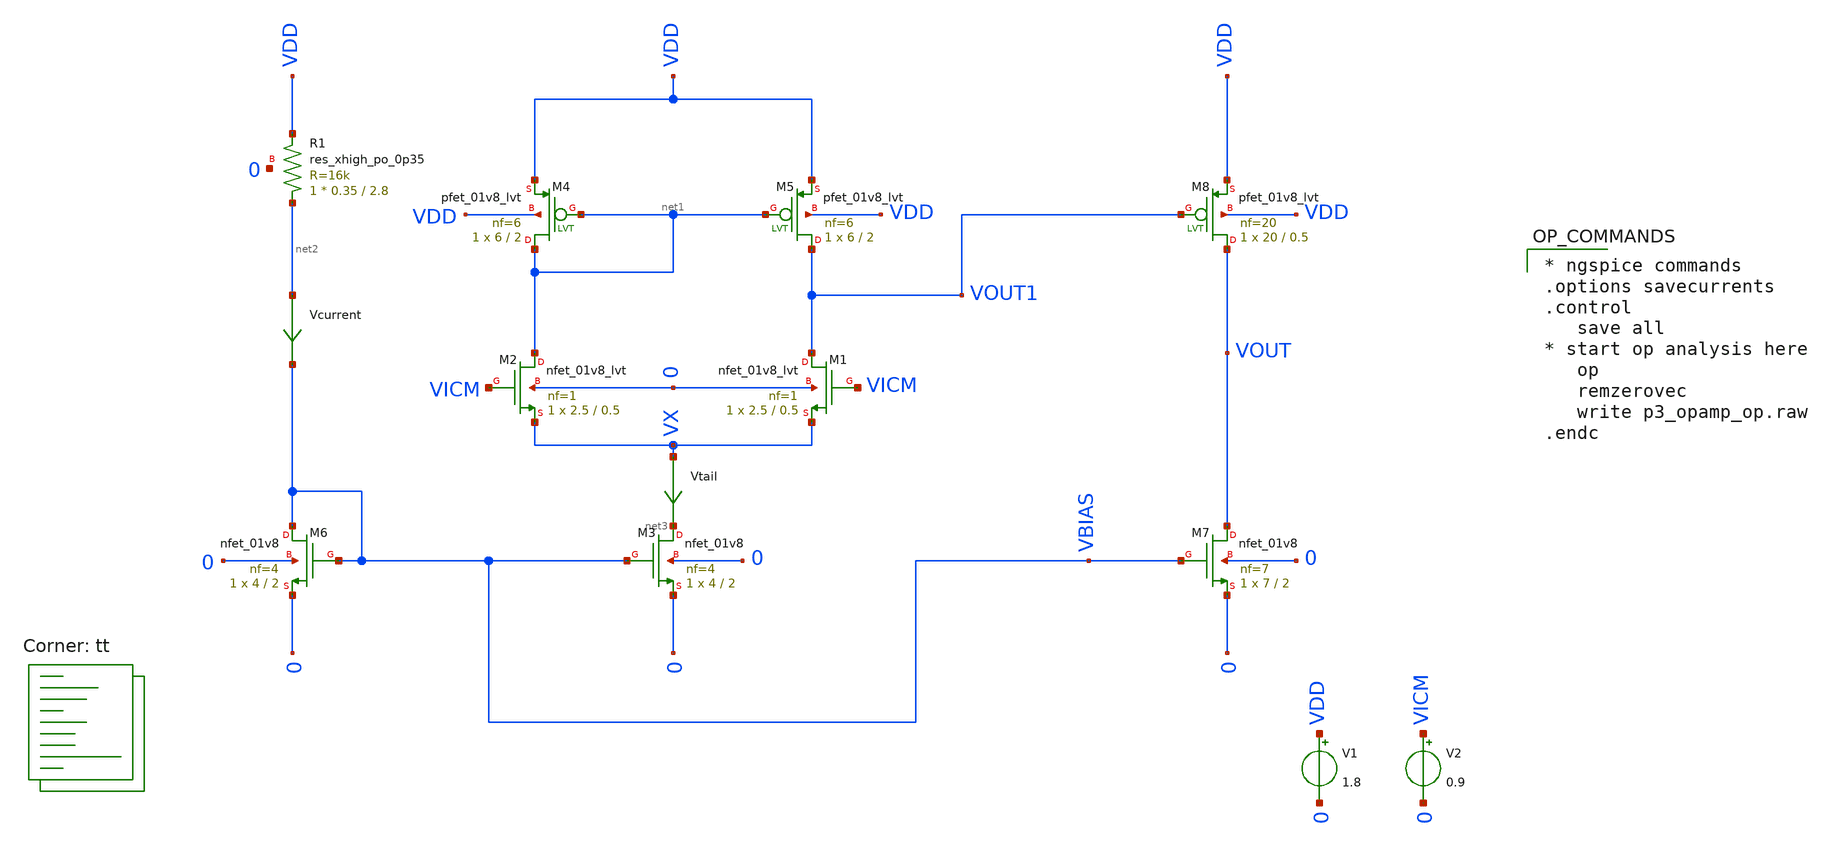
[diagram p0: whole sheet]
** sch_path: xschem/p3_opamp_op.sch
**.subckt p3_opamp_op
XM3 net3 VBIAS 0 0 sky130_fd_pr__nfet_01v8 L=2 W=4 nf=4 ad='int((nf+1)/2) * W/nf * 0.29' as='int((nf+2)/2) * W/nf * 0.29'
+ pd='2*int((nf+1)/2) * (W/nf + 0.29)' ps='2*int((nf+2)/2) * (W/nf + 0.29)' nrd='0.29 / W' nrs='0.29 / W'
+ sa=0 sb=0 sd=0 mult=1 m=1
XM6 VBIAS VBIAS 0 0 sky130_fd_pr__nfet_01v8 L=2 W=4 nf=4 ad='int((nf+1)/2) * W/nf * 0.29' as='int((nf+2)/2) * W/nf * 0.29'
+ pd='2*int((nf+1)/2) * (W/nf + 0.29)' ps='2*int((nf+2)/2) * (W/nf + 0.29)' nrd='0.29 / W' nrs='0.29 / W'
+ sa=0 sb=0 sd=0 mult=1 m=1
XM7 VOUT VBIAS 0 0 sky130_fd_pr__nfet_01v8 L=2 W=7 nf=7 ad='int((nf+1)/2) * W/nf * 0.29' as='int((nf+2)/2) * W/nf * 0.29'
+ pd='2*int((nf+1)/2) * (W/nf + 0.29)' ps='2*int((nf+2)/2) * (W/nf + 0.29)' nrd='0.29 / W' nrs='0.29 / W'
+ sa=0 sb=0 sd=0 mult=1 m=1
V1 VDD 0 1.8
V2 VICM 0 0.9
XR1 net2 VDD 0 sky130_fd_pr__res_xhigh_po_0p35 L=2.8 mult=1 m=1
Vcurrent net2 VBIAS 0
.save i(vcurrent)
Vtail VX net3 0
.save i(vtail)
XM2 net1 VICM VX 0 sky130_fd_pr__nfet_01v8_lvt L=0.5 W=2.5 nf=1 ad='int((nf+1)/2) * W/nf * 0.29' as='int((nf+2)/2) * W/nf * 0.29'
+ pd='2*int((nf+1)/2) * (W/nf + 0.29)' ps='2*int((nf+2)/2) * (W/nf + 0.29)' nrd='0.29 / W' nrs='0.29 / W'
+ sa=0 sb=0 sd=0 mult=1 m=1
XM1 VOUT1 VICM VX 0 sky130_fd_pr__nfet_01v8_lvt L=0.5 W=2.5 nf=1 ad='int((nf+1)/2) * W/nf * 0.29' as='int((nf+2)/2) * W/nf * 0.29'
+ pd='2*int((nf+1)/2) * (W/nf + 0.29)' ps='2*int((nf+2)/2) * (W/nf + 0.29)' nrd='0.29 / W' nrs='0.29 / W'
+ sa=0 sb=0 sd=0 mult=1 m=1
XM4 net1 net1 VDD VDD sky130_fd_pr__pfet_01v8_lvt L=2 W=6 nf=6 ad='int((nf+1)/2) * W/nf * 0.29' as='int((nf+2)/2) * W/nf * 0.29'
+ pd='2*int((nf+1)/2) * (W/nf + 0.29)' ps='2*int((nf+2)/2) * (W/nf + 0.29)' nrd='0.29 / W' nrs='0.29 / W'
+ sa=0 sb=0 sd=0 mult=1 m=1
XM5 VOUT1 net1 VDD VDD sky130_fd_pr__pfet_01v8_lvt L=2 W=6 nf=6 ad='int((nf+1)/2) * W/nf * 0.29' as='int((nf+2)/2) * W/nf * 0.29'
+ pd='2*int((nf+1)/2) * (W/nf + 0.29)' ps='2*int((nf+2)/2) * (W/nf + 0.29)' nrd='0.29 / W' nrs='0.29 / W'
+ sa=0 sb=0 sd=0 mult=1 m=1
XM8 VOUT VOUT1 VDD VDD sky130_fd_pr__pfet_01v8_lvt L=0.5 W=20 nf=20 ad='int((nf+1)/2) * W/nf * 0.29'
+ as='int((nf+2)/2) * W/nf * 0.29' pd='2*int((nf+1)/2) * (W/nf + 0.29)' ps='2*int((nf+2)/2) * (W/nf + 0.29)'
+ nrd='0.29 / W' nrs='0.29 / W' sa=0 sb=0 sd=0 mult=1 m=1
**** begin user architecture code

* ngspice commands
.options savecurrents
.control
   save all
* start op analysis here
   op
   remzerovec
   write p3_opamp_op.raw
.endc


.lib $::SKYWATER_MODELS/sky130.lib.spice tt
**** end user architecture code
**.ends
.end
